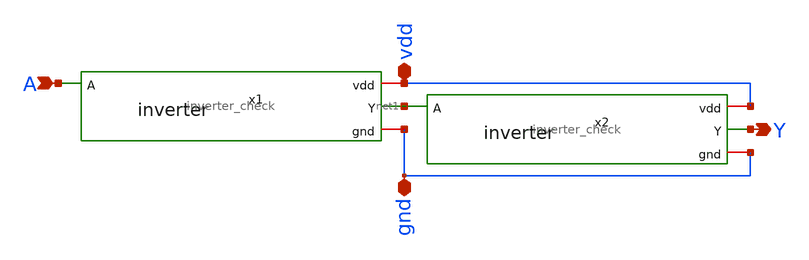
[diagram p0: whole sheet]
** sch_path: Circuit Files/circuits/first_test/buffer.sch
**.subckt buffer A Y vdd gnd
*.ipin A
*.opin Y
*.iopin vdd
*.iopin gnd
x1 vdd A net1 gnd inverter_check
x2 vdd net1 Y gnd inverter_check
**.ends

* expanding   symbol:  daVLSI_World/first_test/inverter_check.sym # of pins=4
** sym_path: Circuit Files/circuits/first_test/inverter_check.sym
** sch_path: Circuit Files/circuits/first_test/inverter_check.sch
.subckt inverter_check vdd A Y gnd
*.ipin A
*.opin Y
*.iopin vdd
*.iopin gnd
XM2 Y A vdd vdd sky130_fd_pr__pfet_01v8 L=0.15 W=2 nf=1 ad='int((nf+1)/2) * W/nf * 0.29' as='int((nf+2)/2) * W/nf * 0.29'
+ pd='2*int((nf+1)/2) * (W/nf + 0.29)' ps='2*int((nf+2)/2) * (W/nf + 0.29)' nrd='0.29 / W' nrs='0.29 / W'
+ sa=0 sb=0 sd=0 mult=1 m=1
XM1 Y A gnd gnd sky130_fd_pr__nfet_01v8 L=0.15 W=1 nf=1 ad='int((nf+1)/2) * W/nf * 0.29' as='int((nf+2)/2) * W/nf * 0.29'
+ pd='2*int((nf+1)/2) * (W/nf + 0.29)' ps='2*int((nf+2)/2) * (W/nf + 0.29)' nrd='0.29 / W' nrs='0.29 / W'
+ sa=0 sb=0 sd=0 mult=1 m=1
.ends

.end
